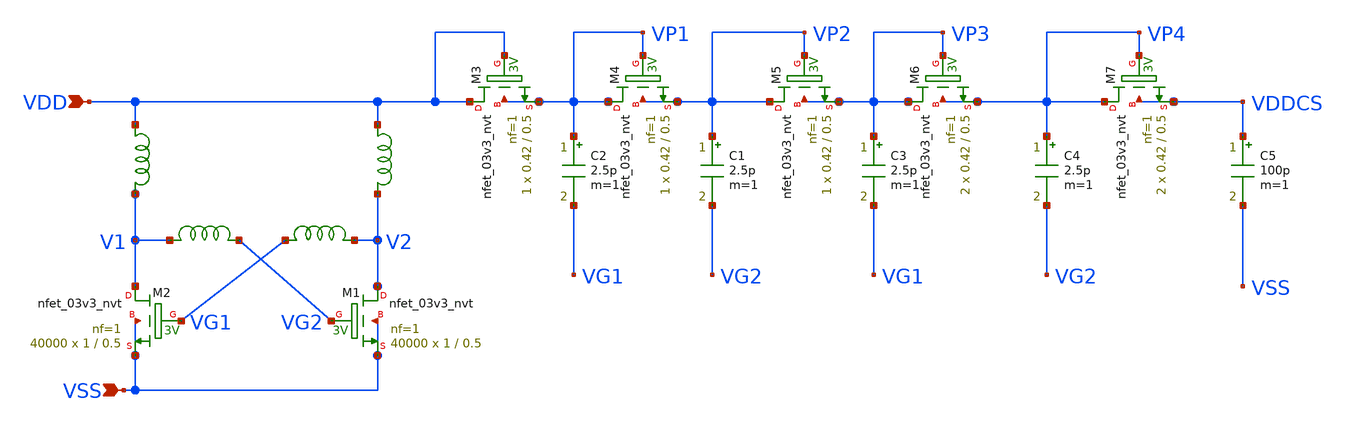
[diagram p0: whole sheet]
** sch_path: design/LELO_SVOD_SKY130A/LELO_EXSC_CHARGE_PUMP.sch
**.subckt LELO_EXSC_CHARGE_PUMP VSS VDD
*.ipin VSS
*.ipin VDD
C1 VP2 VG2 2.5p m=1
C2 VP1 VG1 2.5p m=1
XM3 VDD VDD VP1 VP1 sky130_fd_pr__nfet_03v3_nvt L=0.5 W=0.42 nf=1 ad='int((1 + 1)/2) * 0.42 / 1 * 0.29'
+ as='int((1 + 2)/2) * 0.42 / 1 * 0.29' pd='2*int((1 + 1)/2) * (0.42 / 1 + 0.29)' ps='2*int((1 + 2)/2) * (0.42 / 1 + 0.29)'
+ nrd='0.29 / 0.42 ' nrs='0.29 / 0.42 ' sa=0 sb=0 sd=0 mult=1 m=1
XM1 V2 VG2 VSS VSS sky130_fd_pr__nfet_03v3_nvt L=0.5 W=1 nf=1 ad='int((1 + 1)/2) * 1 / 1 * 0.29' as='int((1 + 2)/2) * 1 / 1 * 0.29'
+ pd='2*int((1 + 1)/2) * (1 / 1 + 0.29)' ps='2*int((1 + 2)/2) * (1 / 1 + 0.29)' nrd='0.29 / 1 ' nrs='0.29 / 1 '
+ sa=0 sb=0 sd=0 mult=40000 m=40000
XM2 V1 VG1 VSS VSS sky130_fd_pr__nfet_03v3_nvt L=0.5 W=1 nf=1 ad='int((1 + 1)/2) * 1 / 1 * 0.29' as='int((1 + 2)/2) * 1 / 1 * 0.29'
+ pd='2*int((1 + 1)/2) * (1 / 1 + 0.29)' ps='2*int((1 + 2)/2) * (1 / 1 + 0.29)' nrd='0.29 / 1 ' nrs='0.29 / 1 '
+ sa=0 sb=0 sd=0 mult=40000 m=40000
XM4 VP1 VP1 VP2 VP2 sky130_fd_pr__nfet_03v3_nvt L=0.5 W=0.42 nf=1 ad='int((1 + 1)/2) * 0.42 / 1 * 0.29'
+ as='int((1 + 2)/2) * 0.42 / 1 * 0.29' pd='2*int((1 + 1)/2) * (0.42 / 1 + 0.29)' ps='2*int((1 + 2)/2) * (0.42 / 1 + 0.29)'
+ nrd='0.29 / 0.42 ' nrs='0.29 / 0.42 ' sa=0 sb=0 sd=0 mult=1 m=1
XM5 VP2 VP2 VP3 VP3 sky130_fd_pr__nfet_03v3_nvt L=0.5 W=0.42 nf=1 ad='int((1 + 1)/2) * 0.42 / 1 * 0.29'
+ as='int((1 + 2)/2) * 0.42 / 1 * 0.29' pd='2*int((1 + 1)/2) * (0.42 / 1 + 0.29)' ps='2*int((1 + 2)/2) * (0.42 / 1 + 0.29)'
+ nrd='0.29 / 0.42 ' nrs='0.29 / 0.42 ' sa=0 sb=0 sd=0 mult=1 m=1
C3 VP3 VG1 2.5p m=1
XM6 VP3 VP3 VP4 VP4 sky130_fd_pr__nfet_03v3_nvt L=0.5 W=0.42 nf=1 ad='int((1 + 1)/2) * 0.42 / 1 * 0.29'
+ as='int((1 + 2)/2) * 0.42 / 1 * 0.29' pd='2*int((1 + 1)/2) * (0.42 / 1 + 0.29)' ps='2*int((1 + 2)/2) * (0.42 / 1 + 0.29)'
+ nrd='0.29 / 0.42 ' nrs='0.29 / 0.42 ' sa=0 sb=0 sd=0 mult=2 m=2
C4 VP4 VG2 2.5p m=1
XM7 VP4 VP4 VDDCS VDDCS sky130_fd_pr__nfet_03v3_nvt L=0.5 W=0.42 nf=1 ad='int((1 + 1)/2) * 0.42 / 1 * 0.29'
+ as='int((1 + 2)/2) * 0.42 / 1 * 0.29' pd='2*int((1 + 1)/2) * (0.42 / 1 + 0.29)' ps='2*int((1 + 2)/2) * (0.42 / 1 + 0.29)'
+ nrd='0.29 / 0.42 ' nrs='0.29 / 0.42 ' sa=0 sb=0 sd=0 mult=2 m=2
C5 VDDCS VSS 100p m=1
x1 V1 VG2 1812PS-334_imp
x2 VG1 V2 1812PS-334_imp
x3 VDD V2 1812PS-102_imp
x4 VDD V1 1812PS-102_imp
**.ends

* expanding   symbol:  LELO_SVOD_SKY130A/1812PS-334_imp.sym # of pins=2
** sym_path: design/LELO_SVOD_SKY130A/1812PS-334_imp.sym

.subckt 1812PS-334_imp port1 port2
X1 port1 port2 Model1D R1=75 R2=4.9 C= 2.43p K1=1E-06 K2=57.9 K3= 330u K4=0.000001 K5=0.000001 L=0
+ Is=0 a=0 L_Z0=0 L_EL=0 L_F0=0E6 PkZ=127597.141
.ends 1812PS-334_imp


* expanding   symbol:  LELO_SVOD_SKY130A/1812PS-102_imp.sym # of pins=2
** sym_path: design/LELO_SVOD_SKY130A/1812PS-102_imp.sym

.subckt 1812PS-102_imp port1 port2
X1 port1 port2 Model1D R1=60 R2=0.054 C= 0.15p K1=0.000001 K2=0.064 K3= 1u K4=1E-06 K5=0.000001 L=0
+ Is=0 a=0 L_Z0=0 L_EL=0 L_F0=0E6 PkZ=1282.46492
.ends 1812PS-102_imp
.end
